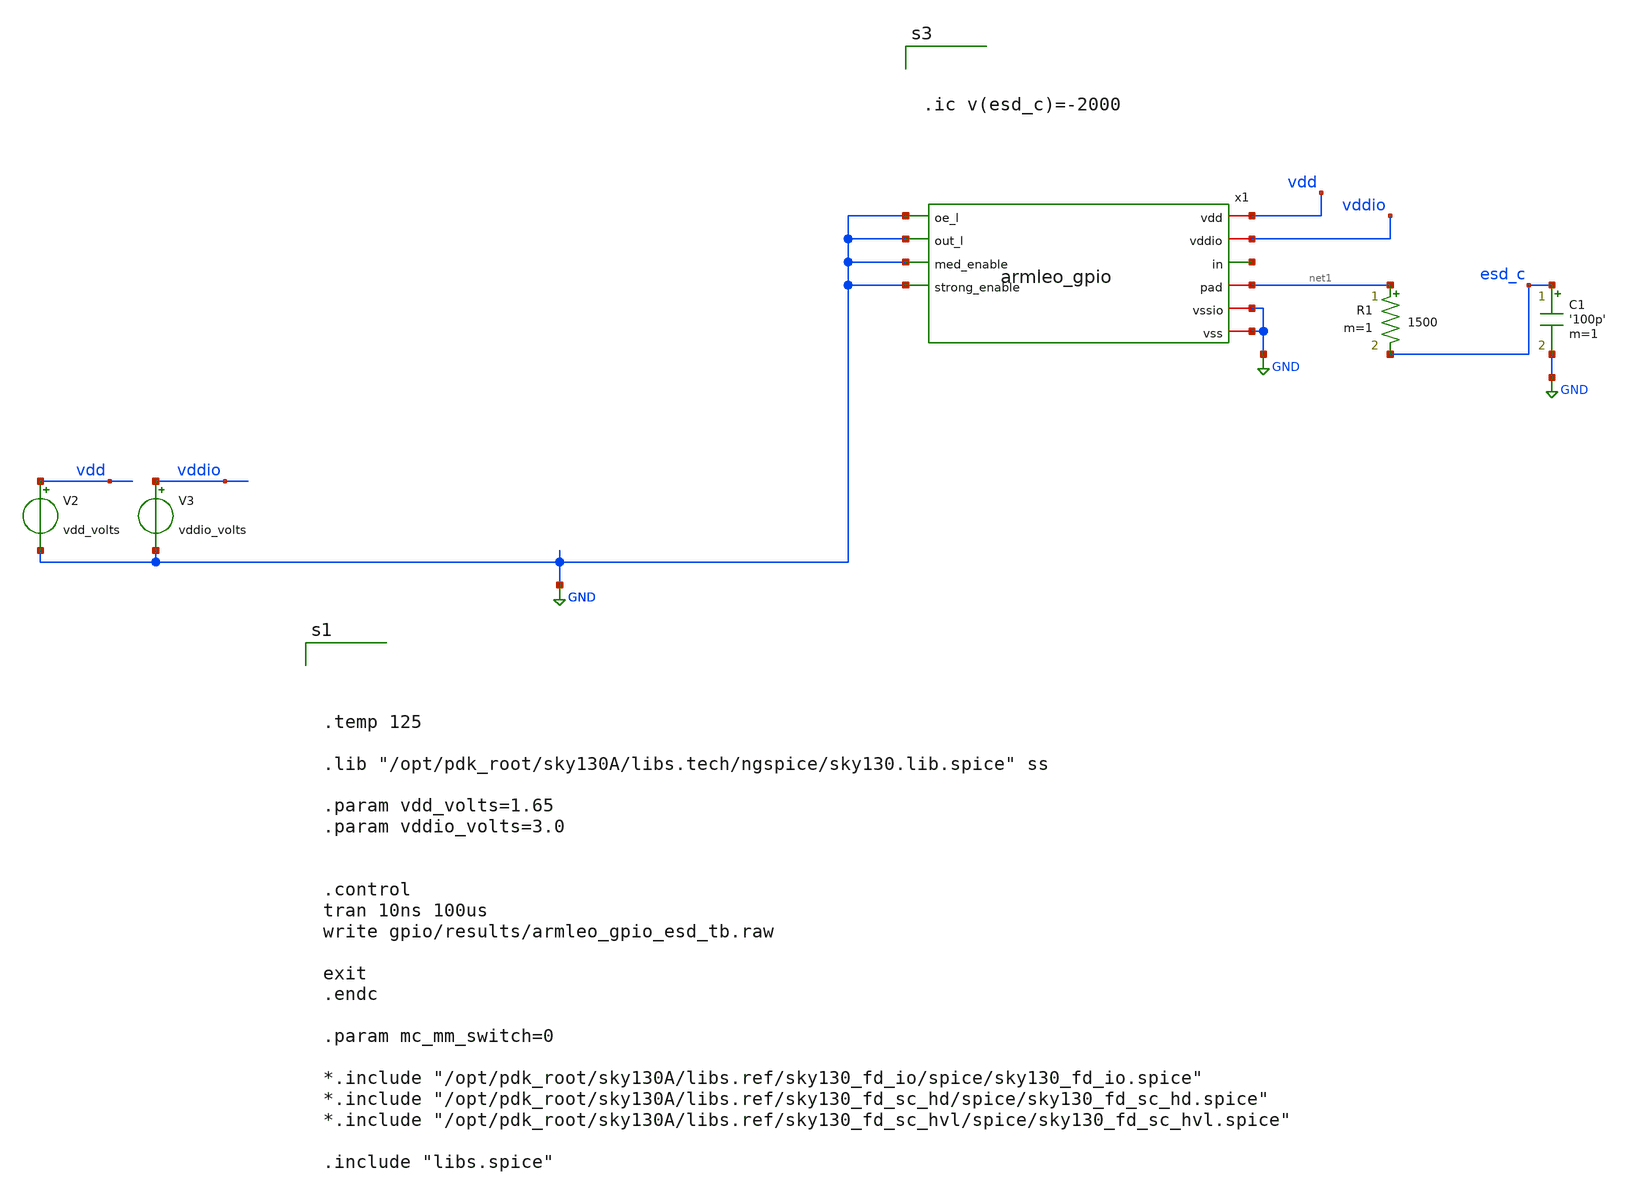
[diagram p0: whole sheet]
** sch_path: xschem/gpio/testbenches/armleo_gpio_esd_tb.sch
**.subckt armleo_gpio_esd_tb
V2 vdd GND vdd_volts
C1 esd_c GND '100p' m=1
V3 vddio GND vddio_volts
x1 vdd vddio net2 net1 GND GND GND GND GND GND armleo_gpio
R1 net1 esd_c 1500 m=1
**** begin user architecture code




.temp 125

.lib "/opt/pdk_root/sky130A/libs.tech/ngspice/sky130.lib.spice" ss

.param vdd_volts=1.65
.param vddio_volts=3.0


.control
tran 10ns 100us
write gpio/results/armleo_gpio_esd_tb.raw

exit
.endc

.param mc_mm_switch=0

*.include "/opt/pdk_root/sky130A/libs.ref/sky130_fd_io/spice/sky130_fd_io.spice"
*.include "/opt/pdk_root/sky130A/libs.ref/sky130_fd_sc_hd/spice/sky130_fd_sc_hd.spice"
*.include "/opt/pdk_root/sky130A/libs.ref/sky130_fd_sc_hvl/spice/sky130_fd_sc_hvl.spice"

.include "libs.spice"






.ic v(esd_c)=-2000


**** end user architecture code
**.ends

* expanding   symbol:  gpio/armleo_gpio.sym # of pins=10
** sym_path: xschem/gpio/armleo_gpio.sym
** sch_path: xschem/gpio/armleo_gpio.sch
.subckt armleo_gpio vdd vddio in pad oe_l out_l med_enable strong_enable vssio vss
*.ipin out_l
*.iopin vddio
*.iopin vssio
*.ipin oe_l
*.opin in
*.iopin vdd
*.iopin vss
*.iopin pad
*.ipin med_enable
*.ipin strong_enable
x2 vddio n1 weak_pgate n2 vssio armleo_gpio_lv2hv
x6 esd_pad vss vss vdd vdd in sky130_fd_sc_hvl__buf_16
x37 vddio n3 weak_ngate n4 vssio armleo_gpio_lv2hv
XM1 pad m2_weak_pgate vddio vddio sky130_fd_pr__pfet_g5v0d10v5 L=0.5 W=10 nf=1 ad='int((nf+1)/2) * W/nf * 0.29'
+ as='int((nf+2)/2) * W/nf * 0.29' pd='2*int((nf+1)/2) * (W/nf + 0.29)' ps='2*int((nf+2)/2) * (W/nf + 0.29)'
+ nrd='0.29 / W' nrs='0.29 / W' sa=0 sb=0 sd=0 mult=3*2 m=3*2
XM2 pad m2_weak_ngate vssio vssio sky130_fd_pr__nfet_g5v0d10v5 L=0.5 W=4.5 nf=1 ad='int((nf+1)/2) * W/nf * 0.29'
+ as='int((nf+2)/2) * W/nf * 0.29' pd='2*int((nf+1)/2) * (W/nf + 0.29)' ps='2*int((nf+2)/2) * (W/nf + 0.29)'
+ nrd='0.29 / W' nrs='0.29 / W' sa=0 sb=0 sd=0 mult=3*2 m=3*2
x1 weak_ngate vssio vssio vddio vddio m1_weak_ngate_n sky130_fd_sc_hvl__inv_4
x5 weak_pgate vssio vssio vddio vddio m1_weak_pgate_n sky130_fd_sc_hvl__inv_4
x3 m1_weak_pgate_n vssio vssio vddio vddio m2_weak_pgate sky130_fd_sc_hvl__inv_16
x10 m1_weak_ngate_n vssio vssio vddio vddio m2_weak_ngate sky130_fd_sc_hvl__inv_16
x8 n3 vss vss vdd vdd n4 sky130_fd_sc_hd__inv_4
x12 n1 vss vss vdd vdd n2 sky130_fd_sc_hd__inv_4
x14 oe_l vss vss vdd vdd n5 sky130_fd_sc_hd__inv_4
x16 oe_l out_l vss vss vdd vdd n1 sky130_fd_sc_hd__nand2_4
x17 out_l n5 vss vss vdd vdd n3 sky130_fd_sc_hd__nor2_4
R1 pad esd_pad sky130_fd_pr__res_generic_l1 W=1 L=10 m=1
x4 vddio n1_med med_pgate n2_med vssio armleo_gpio_lv2hv
x7 vddio n3_med med_ngate n4_med vssio armleo_gpio_lv2hv
x9 n3_med vss vss vdd vdd n4_med sky130_fd_sc_hd__inv_4
x11 n1_med vss vss vdd vdd n2_med sky130_fd_sc_hd__inv_4
x13 vddio n1_strong strong_pgate n2_strong vssio armleo_gpio_lv2hv
x15 vddio n3_strong strong_ngate n4_strong vssio armleo_gpio_lv2hv
x18 n3_strong vss vss vdd vdd n4_strong sky130_fd_sc_hd__inv_4
x19 n1_strong vss vss vdd vdd n2_strong sky130_fd_sc_hd__inv_4
XM3 pad m2_med_pgate vddio vddio sky130_fd_pr__pfet_g5v0d10v5 L=0.5 W=10 nf=1 ad='int((nf+1)/2) * W/nf * 0.29'
+ as='int((nf+2)/2) * W/nf * 0.29' pd='2*int((nf+1)/2) * (W/nf + 0.29)' ps='2*int((nf+2)/2) * (W/nf + 0.29)'
+ nrd='0.29 / W' nrs='0.29 / W' sa=0 sb=0 sd=0 mult=3*3 m=3*3
XM4 pad m2_med_ngate vssio vssio sky130_fd_pr__nfet_g5v0d10v5 L=0.5 W=4.5 nf=1 ad='int((nf+1)/2) * W/nf * 0.29'
+ as='int((nf+2)/2) * W/nf * 0.29' pd='2*int((nf+1)/2) * (W/nf + 0.29)' ps='2*int((nf+2)/2) * (W/nf + 0.29)'
+ nrd='0.29 / W' nrs='0.29 / W' sa=0 sb=0 sd=0 mult=3*3 m=3*3
x20 med_ngate vssio vssio vddio vddio m1_med_ngate_n sky130_fd_sc_hvl__inv_4
x21 med_pgate vssio vssio vddio vddio m1_med_pgate_n sky130_fd_sc_hvl__inv_4
x22 m1_med_pgate_n vssio vssio vddio vddio m2_med_pgate sky130_fd_sc_hvl__inv_16
x23 m1_med_ngate_n vssio vssio vddio vddio m2_med_ngate sky130_fd_sc_hvl__inv_16
x24 n6_med vss vss vdd vdd n5_med sky130_fd_sc_hd__inv_4
x25 n5_med out_l vss vss vdd vdd n1_med sky130_fd_sc_hd__nand2_4
x26 out_l n6_med vss vss vdd vdd n3_med sky130_fd_sc_hd__nor2_4
x28 net1 vss vss vdd vdd n5_strong sky130_fd_sc_hd__inv_4
x29 n5_strong out_l vss vss vdd vdd n1_strong sky130_fd_sc_hd__nand2_4
x30 out_l net1 vss vss vdd vdd n3_strong sky130_fd_sc_hd__nor2_4
XM7 pad m2_strong_pgate vddio vddio sky130_fd_pr__pfet_g5v0d10v5 L=0.5 W=10 nf=1 ad='int((nf+1)/2) * W/nf * 0.29'
+ as='int((nf+2)/2) * W/nf * 0.29' pd='2*int((nf+1)/2) * (W/nf + 0.29)' ps='2*int((nf+2)/2) * (W/nf + 0.29)'
+ nrd='0.29 / W' nrs='0.29 / W' sa=0 sb=0 sd=0 mult=3*7 m=3*7
XM8 pad m2_strong_ngate vssio vssio sky130_fd_pr__nfet_g5v0d10v5 L=0.5 W=4.5 nf=1 ad='int((nf+1)/2) * W/nf * 0.29'
+ as='int((nf+2)/2) * W/nf * 0.29' pd='2*int((nf+1)/2) * (W/nf + 0.29)' ps='2*int((nf+2)/2) * (W/nf + 0.29)'
+ nrd='0.29 / W' nrs='0.29 / W' sa=0 sb=0 sd=0 mult=3*7 m=3*7
x36 strong_ngate vssio vssio vddio vddio m1_strong_ngate_n sky130_fd_sc_hvl__inv_4
x38 strong_pgate vssio vssio vddio vddio m1_strong_pgate_n sky130_fd_sc_hvl__inv_4
x39 m1_strong_pgate_n vssio vssio vddio vddio m2_strong_pgate sky130_fd_sc_hvl__inv_16
x40 m1_strong_ngate_n vssio vssio vddio vddio m2_strong_ngate sky130_fd_sc_hvl__inv_16
XM9 pad vssio vssio vssio sky130_fd_pr__esd_nfet_g5v0d10v5 L=0.6 W=5.4 nf=1 ad='int((nf+1)/2) * W/nf * 0.29'
+ as='int((nf+2)/2) * W/nf * 0.29' pd='2*int((nf+1)/2) * (W/nf + 0.29)' ps='2*int((nf+2)/2) * (W/nf + 0.29)'
+ nrd='0.29 / W' nrs='0.29 / W' sa=0 sb=0 sd=0 mult=12 m=12
x27 oe_l med_enable vss vss vdd vdd n6_med sky130_fd_sc_hd__nand2_4
x31 oe_l strong_enable vss vss vdd vdd net1 sky130_fd_sc_hd__nand2_4
.ends


* expanding   symbol:  gpio/armleo_gpio_lv2hv.sym # of pins=5
** sym_path: xschem/gpio/armleo_gpio_lv2hv.sym
** sch_path: xschem/gpio/armleo_gpio_lv2hv.sch
.subckt armleo_gpio_lv2hv VDDH A Y A_N VSSH
*.ipin A
*.iopin VDDH
*.iopin VSSH
*.opin Y
*.ipin A_N
XM2 VSSH A_N Y VSSH sky130_fd_pr__nfet_g5v0d10v5 L=0.5 W=1 nf=1 ad='int((nf+1)/2) * W/nf * 0.29' as='int((nf+2)/2) * W/nf * 0.29'
+ pd='2*int((nf+1)/2) * (W/nf + 0.29)' ps='2*int((nf+2)/2) * (W/nf + 0.29)' nrd='0.29 / W' nrs='0.29 / W'
+ sa=0 sb=0 sd=0 mult=1 m=1
XM5 N1 A VSSH VSSH sky130_fd_pr__nfet_g5v0d10v5 L=0.5 W=1 nf=1 ad='int((nf+1)/2) * W/nf * 0.29' as='int((nf+2)/2) * W/nf * 0.29'
+ pd='2*int((nf+1)/2) * (W/nf + 0.29)' ps='2*int((nf+2)/2) * (W/nf + 0.29)' nrd='0.29 / W' nrs='0.29 / W'
+ sa=0 sb=0 sd=0 mult=1 m=1
XM4 VDDH Y N2 VDDH sky130_fd_pr__pfet_g5v0d10v5 L=0.5 W=1 nf=1 ad='int((nf+1)/2) * W/nf * 0.29' as='int((nf+2)/2) * W/nf * 0.29'
+ pd='2*int((nf+1)/2) * (W/nf + 0.29)' ps='2*int((nf+2)/2) * (W/nf + 0.29)' nrd='0.29 / W' nrs='0.29 / W'
+ sa=0 sb=0 sd=0 mult=1 m=1
XM7 net1 N1 VDDH VDDH sky130_fd_pr__pfet_g5v0d10v5 L=0.5 W=1 nf=1 ad='int((nf+1)/2) * W/nf * 0.29' as='int((nf+2)/2) * W/nf * 0.29'
+ pd='2*int((nf+1)/2) * (W/nf + 0.29)' ps='2*int((nf+2)/2) * (W/nf + 0.29)' nrd='0.29 / W' nrs='0.29 / W'
+ sa=0 sb=0 sd=0 mult=1 m=1
XM9 N1 A N2 VDDH sky130_fd_pr__pfet_g5v0d10v5 L=0.5 W=1 nf=1 ad='int((nf+1)/2) * W/nf * 0.29' as='int((nf+2)/2) * W/nf * 0.29'
+ pd='2*int((nf+1)/2) * (W/nf + 0.29)' ps='2*int((nf+2)/2) * (W/nf + 0.29)' nrd='0.29 / W' nrs='0.29 / W'
+ sa=0 sb=0 sd=0 mult=1 m=1
XM11 net1 A_N Y VDDH sky130_fd_pr__pfet_g5v0d10v5 L=0.5 W=1 nf=1 ad='int((nf+1)/2) * W/nf * 0.29' as='int((nf+2)/2) * W/nf * 0.29'
+ pd='2*int((nf+1)/2) * (W/nf + 0.29)' ps='2*int((nf+2)/2) * (W/nf + 0.29)' nrd='0.29 / W' nrs='0.29 / W'
+ sa=0 sb=0 sd=0 mult=1 m=1
.ends

.GLOBAL GND
.end
